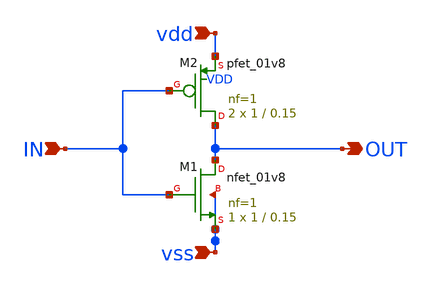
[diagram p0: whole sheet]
** sch_path: inverter.sch
**.subckt inverter OUT IN vdd vss
*.opin OUT
*.ipin IN
*.ipin vdd
*.ipin vss
XM1 OUT IN vss vss sky130_fd_pr__nfet_01v8 L=0.15 W=1 nf=1 ad='int((nf+1)/2) * W/nf * 0.29' as='int((nf+2)/2) * W/nf * 0.29'
+ pd='2*int((nf+1)/2) * (W/nf + 0.29)' ps='2*int((nf+2)/2) * (W/nf + 0.29)' nrd='0.29 / W' nrs='0.29 / W'
+ sa=0 sb=0 sd=0 mult=1 m=1
XM2 OUT IN vdd VDD sky130_fd_pr__pfet_01v8 L=0.15 W=1 nf=1 ad='int((nf+1)/2) * W/nf * 0.29' as='int((nf+2)/2) * W/nf * 0.29'
+ pd='2*int((nf+1)/2) * (W/nf + 0.29)' ps='2*int((nf+2)/2) * (W/nf + 0.29)' nrd='0.29 / W' nrs='0.29 / W'
+ sa=0 sb=0 sd=0 mult=2 m=2
**.ends
.end
